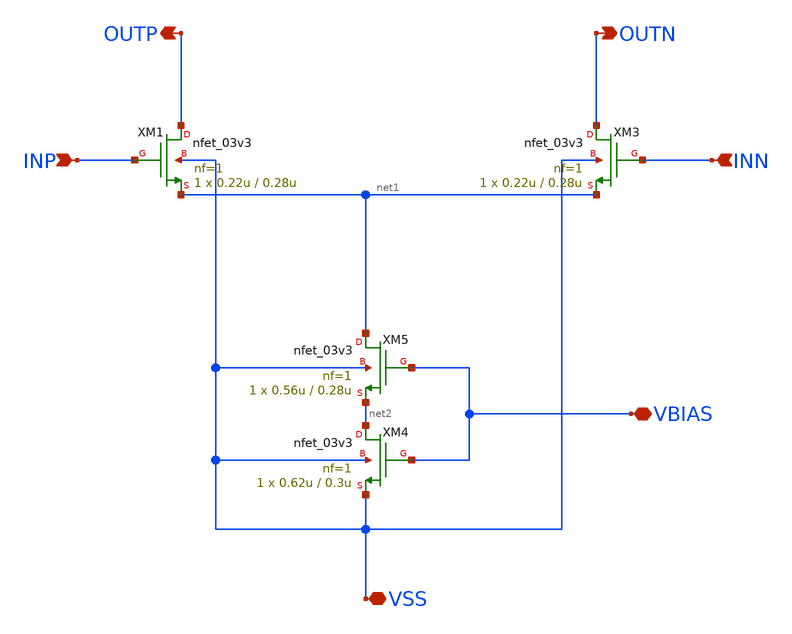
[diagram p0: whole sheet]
** sch_path: xschem/CS_Switch_8x2.sch
**.subckt CS_Switch_8x2 INP INN OUTP OUTN VBIAS VSS
*.ipin INP
*.ipin INN
*.opin OUTP
*.opin OUTN
*.iopin VBIAS
*.iopin VSS
XM5 net1 VBIAS net2 VSS nfet_03v3 L=0.28u W=0.56u nf=1 ad='int((nf+1)/2) * W/nf * 0.18u' as='int((nf+2)/2) * W/nf * 0.18u'
+ pd='2*int((nf+1)/2) * (W/nf + 0.18u)' ps='2*int((nf+2)/2) * (W/nf + 0.18u)' nrd='0.18u / W' nrs='0.18u / W'
+ sa=0 sb=0 sd=0 m=1
XM4 net2 VBIAS VSS VSS nfet_03v3 L=0.3u W=0.62u nf=1 ad='int((nf+1)/2) * W/nf * 0.18u' as='int((nf+2)/2) * W/nf * 0.18u'
+ pd='2*int((nf+1)/2) * (W/nf + 0.18u)' ps='2*int((nf+2)/2) * (W/nf + 0.18u)' nrd='0.18u / W' nrs='0.18u / W'
+ sa=0 sb=0 sd=0 m=1
XM1 OUTP INP net1 VSS nfet_03v3 L=0.28u W=0.22u nf=1 ad='int((nf+1)/2) * W/nf * 0.18u' as='int((nf+2)/2) * W/nf * 0.18u'
+ pd='2*int((nf+1)/2) * (W/nf + 0.18u)' ps='2*int((nf+2)/2) * (W/nf + 0.18u)' nrd='0.18u / W' nrs='0.18u / W'
+ sa=0 sb=0 sd=0 m=1
XM3 OUTN INN net1 VSS nfet_03v3 L=0.28u W=0.22u nf=1 ad='int((nf+1)/2) * W/nf * 0.18u' as='int((nf+2)/2) * W/nf * 0.18u'
+ pd='2*int((nf+1)/2) * (W/nf + 0.18u)' ps='2*int((nf+2)/2) * (W/nf + 0.18u)' nrd='0.18u / W' nrs='0.18u / W'
+ sa=0 sb=0 sd=0 m=1
**.ends
.end
